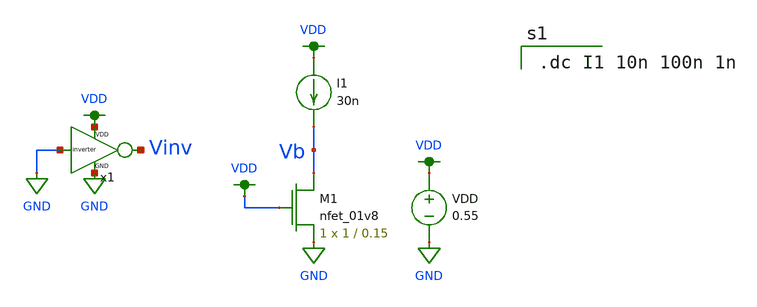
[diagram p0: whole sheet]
** sch_path: schematics/Extra files/test_nmos.sch
**.subckt test_nmos
XM1 Vb VDD GND GND sky130_fd_pr__nfet_01v8 L=0.15 W=1 nf=1 ad='int((nf+1)/2) * W/nf * 0.29' as='int((nf+2)/2) * W/nf * 0.29'
+ pd='2*int((nf+1)/2) * (W/nf + 0.29)' ps='2*int((nf+2)/2) * (W/nf + 0.29)' nrd='0.29 / W' nrs='0.29 / W'
+ sa=0 sb=0 sd=0 mult=1 m=1
VDD VDD GND 0.55
I1 VDD Vb 30n
x1 VDD GND Vinv GND inverter
**** begin user architecture code

.option wnflag=1
.param MC_SWITCH=0.0
.lib ~/skywater/skywater-pdk/libraries/sky130_fd_pr_ngspice/latest/models/sky130.lib.spice tt


.dc I1 10n 100n 1n

**** end user architecture code
**.ends

* expanding   symbol:  /home/madvlsi/dev/git/7-bit-D-A-converter-MP4-MADVLSI/schematics/ieee
*+ DAC/inverter.sym # of pins=4
** sym_path: schematics/ieee DAC/inverter.sym
** sch_path: schematics/ieee DAC/inverter.sch
.subckt inverter VDD A Y GND
*.ipin A
*.iopin VDD
*.iopin GND
*.opin Y
XM1 Y A GND GND sky130_fd_pr__nfet_01v8 L=0.5 W=12 nf=1 ad='int((nf+1)/2) * W/nf * 0.29' as='int((nf+2)/2) * W/nf * 0.29'
+ pd='2*int((nf+1)/2) * (W/nf + 0.29)' ps='2*int((nf+2)/2) * (W/nf + 0.29)' nrd='0.29 / W' nrs='0.29 / W'
+ sa=0 sb=0 sd=0 mult=1 m=1
XM2 Y A VDD VDD sky130_fd_pr__pfet_01v8 L=0.5 W=12 nf=1 ad='int((nf+1)/2) * W/nf * 0.29' as='int((nf+2)/2) * W/nf * 0.29'
+ pd='2*int((nf+1)/2) * (W/nf + 0.29)' ps='2*int((nf+2)/2) * (W/nf + 0.29)' nrd='0.29 / W' nrs='0.29 / W'
+ sa=0 sb=0 sd=0 mult=1 m=1
.ends

.GLOBAL VDD
.GLOBAL GND
.end
